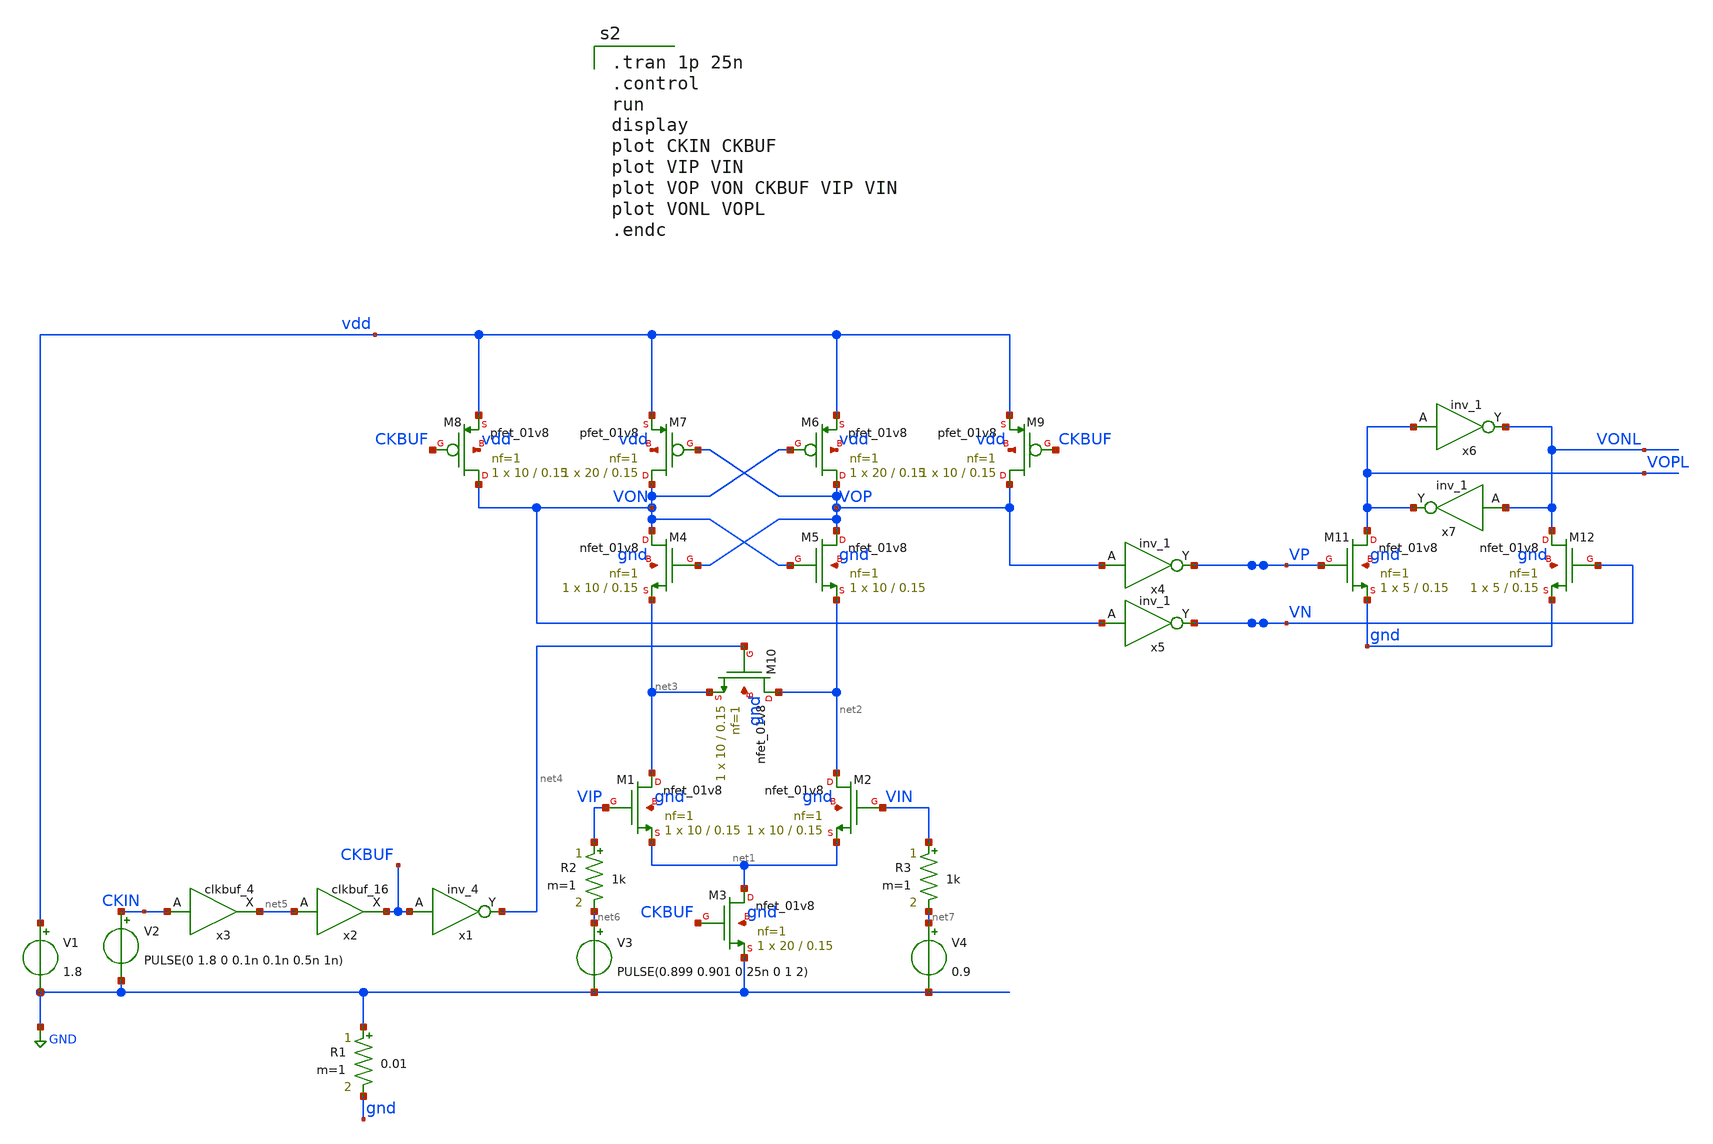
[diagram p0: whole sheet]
** sch_path: xschem/adc_strongarm.sch
**.subckt adc_strongarm
XM1 net3 VIP net1 gnd sky130_fd_pr__nfet_01v8 L=0.15 W=10 nf=1 ad='int((nf+1)/2) * W/nf * 0.29' as='int((nf+2)/2) * W/nf * 0.29'
+ pd='2*int((nf+1)/2) * (W/nf + 0.29)' ps='2*int((nf+2)/2) * (W/nf + 0.29)' nrd='0.29 / W' nrs='0.29 / W'
+ sa=0 sb=0 sd=0 mult=1 m=1
XM2 net2 VIN net1 gnd sky130_fd_pr__nfet_01v8 L=0.15 W=10 nf=1 ad='int((nf+1)/2) * W/nf * 0.29' as='int((nf+2)/2) * W/nf * 0.29'
+ pd='2*int((nf+1)/2) * (W/nf + 0.29)' ps='2*int((nf+2)/2) * (W/nf + 0.29)' nrd='0.29 / W' nrs='0.29 / W'
+ sa=0 sb=0 sd=0 mult=1 m=1
XM3 net1 CKBUF GND gnd sky130_fd_pr__nfet_01v8 L=0.15 W=20 nf=1 ad='int((nf+1)/2) * W/nf * 0.29' as='int((nf+2)/2) * W/nf * 0.29'
+ pd='2*int((nf+1)/2) * (W/nf + 0.29)' ps='2*int((nf+2)/2) * (W/nf + 0.29)' nrd='0.29 / W' nrs='0.29 / W'
+ sa=0 sb=0 sd=0 mult=1 m=1
XM4 VON VOP net3 gnd sky130_fd_pr__nfet_01v8 L=0.15 W=10 nf=1 ad='int((nf+1)/2) * W/nf * 0.29' as='int((nf+2)/2) * W/nf * 0.29'
+ pd='2*int((nf+1)/2) * (W/nf + 0.29)' ps='2*int((nf+2)/2) * (W/nf + 0.29)' nrd='0.29 / W' nrs='0.29 / W'
+ sa=0 sb=0 sd=0 mult=1 m=1
XM5 VOP VON net2 gnd sky130_fd_pr__nfet_01v8 L=0.15 W=10 nf=1 ad='int((nf+1)/2) * W/nf * 0.29' as='int((nf+2)/2) * W/nf * 0.29'
+ pd='2*int((nf+1)/2) * (W/nf + 0.29)' ps='2*int((nf+2)/2) * (W/nf + 0.29)' nrd='0.29 / W' nrs='0.29 / W'
+ sa=0 sb=0 sd=0 mult=1 m=1
XM6 VOP VON vdd vdd sky130_fd_pr__pfet_01v8 L=0.15 W=20 nf=1 ad='int((nf+1)/2) * W/nf * 0.29' as='int((nf+2)/2) * W/nf * 0.29'
+ pd='2*int((nf+1)/2) * (W/nf + 0.29)' ps='2*int((nf+2)/2) * (W/nf + 0.29)' nrd='0.29 / W' nrs='0.29 / W'
+ sa=0 sb=0 sd=0 mult=1 m=1
XM7 VON VOP vdd vdd sky130_fd_pr__pfet_01v8 L=0.15 W=20 nf=1 ad='int((nf+1)/2) * W/nf * 0.29' as='int((nf+2)/2) * W/nf * 0.29'
+ pd='2*int((nf+1)/2) * (W/nf + 0.29)' ps='2*int((nf+2)/2) * (W/nf + 0.29)' nrd='0.29 / W' nrs='0.29 / W'
+ sa=0 sb=0 sd=0 mult=1 m=1
XM8 VON CKBUF vdd vdd sky130_fd_pr__pfet_01v8 L=0.15 W=10 nf=1 ad='int((nf+1)/2) * W/nf * 0.29' as='int((nf+2)/2) * W/nf * 0.29'
+ pd='2*int((nf+1)/2) * (W/nf + 0.29)' ps='2*int((nf+2)/2) * (W/nf + 0.29)' nrd='0.29 / W' nrs='0.29 / W'
+ sa=0 sb=0 sd=0 mult=1 m=1
XM9 VOP CKBUF vdd vdd sky130_fd_pr__pfet_01v8 L=0.15 W=10 nf=1 ad='int((nf+1)/2) * W/nf * 0.29' as='int((nf+2)/2) * W/nf * 0.29'
+ pd='2*int((nf+1)/2) * (W/nf + 0.29)' ps='2*int((nf+2)/2) * (W/nf + 0.29)' nrd='0.29 / W' nrs='0.29 / W'
+ sa=0 sb=0 sd=0 mult=1 m=1
V1 vdd GND 1.8
x1 CKBUF gnd gnd vdd vdd net4 sky130_fd_sc_hs__inv_4
XM10 net2 net4 net3 gnd sky130_fd_pr__nfet_01v8 L=0.15 W=10 nf=1 ad='int((nf+1)/2) * W/nf * 0.29' as='int((nf+2)/2) * W/nf * 0.29'
+ pd='2*int((nf+1)/2) * (W/nf + 0.29)' ps='2*int((nf+2)/2) * (W/nf + 0.29)' nrd='0.29 / W' nrs='0.29 / W'
+ sa=0 sb=0 sd=0 mult=1 m=1
x2 net5 gnd gnd vdd vdd CKBUF sky130_fd_sc_hs__clkbuf_16
V2 CKIN GND PULSE(0 1.8 0 0.1n 0.1n 0.5n 1n)
V3 net6 GND PULSE(0.899 0.901 0 25n 0 1 2)
V4 net7 GND 0.9
R1 GND gnd 0.01 m=1
x3 CKIN gnd gnd vdd vdd net5 sky130_fd_sc_hs__clkbuf_4
x4 VOP gnd gnd vdd vdd VP sky130_fd_sc_hs__inv_1
x5 VON gnd gnd vdd vdd VN sky130_fd_sc_hs__inv_1
R2 VIP net6 1k m=1
R3 VIN net7 1k m=1
XM11 VOPL VP gnd gnd sky130_fd_pr__nfet_01v8 L=0.15 W=5 nf=1 ad='int((nf+1)/2) * W/nf * 0.29' as='int((nf+2)/2) * W/nf * 0.29'
+ pd='2*int((nf+1)/2) * (W/nf + 0.29)' ps='2*int((nf+2)/2) * (W/nf + 0.29)' nrd='0.29 / W' nrs='0.29 / W'
+ sa=0 sb=0 sd=0 mult=1 m=1
XM12 VONL VN gnd gnd sky130_fd_pr__nfet_01v8 L=0.15 W=5 nf=1 ad='int((nf+1)/2) * W/nf * 0.29' as='int((nf+2)/2) * W/nf * 0.29'
+ pd='2*int((nf+1)/2) * (W/nf + 0.29)' ps='2*int((nf+2)/2) * (W/nf + 0.29)' nrd='0.29 / W' nrs='0.29 / W'
+ sa=0 sb=0 sd=0 mult=1 m=1
x6 VOPL gnd gnd vdd vdd VONL sky130_fd_sc_hs__inv_1
x7 VONL gnd gnd vdd vdd VOPL sky130_fd_sc_hs__inv_1
**** begin user architecture code

.tran 1p 25n
.control
run
display
plot CKIN CKBUF
plot VIP VIN
plot VOP VON CKBUF VIP VIN
plot VONL VOPL
.endc


.lib $::SKYWATER_MODELS/sky130.lib.spice tt
.include $::PDKPATH/libs.ref/sky130_fd_sc_hs/spice/sky130_fd_sc_hs.spice

**** end user architecture code
**.ends
.GLOBAL GND
.end
